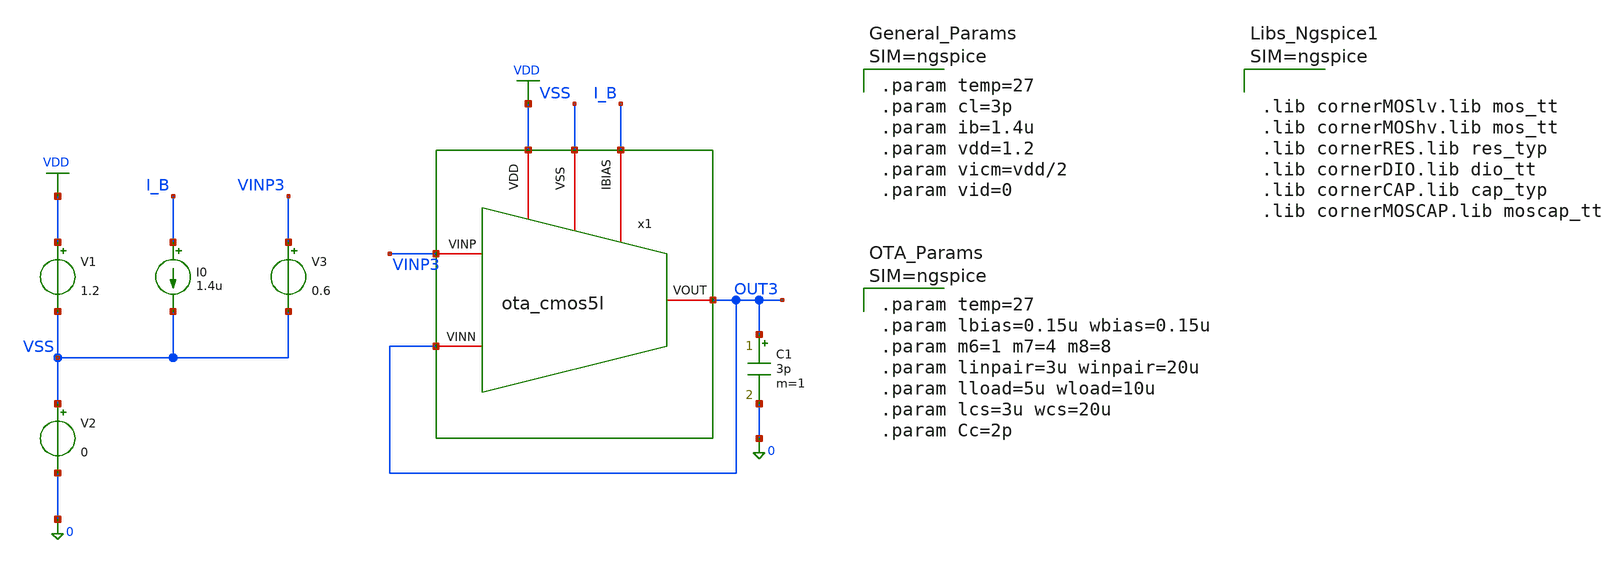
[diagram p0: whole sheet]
** sch_path: xschem/ota_cmos5l/tb/tb_ota_cmos5l_cmrr/tb_ota_cmos5l_cmrr.sch
**.subckt tb_ota_cmos5l_cmrr
x1 VSS I_B VDD OUT3 VINP3 OUT3 ota_cmos5l
C1 OUT3 0 3p m=1
I0 I_B VSS 1.4u
V1 VDD VSS 1.2
V2 VSS 0 0
V3 VINP3 VSS 0.6
**** begin user architecture code



.lib cornerMOSlv.lib mos_tt
.lib cornerMOShv.lib mos_tt
.lib cornerRES.lib res_typ
.lib cornerDIO.lib dio_tt
.lib cornerCAP.lib cap_typ
.lib cornerMOSCAP.lib moscap_tt





.param temp=27
.param cl=3p
.param ib=1.4u
.param vdd=1.2
.param vicm=vdd/2
.param vid=0





.param temp=27
.param lbias=0.15u wbias=0.15u
.param m6=1 m7=4 m8=8
.param linpair=3u winpair=20u
.param lload=5u wload=10u
.param lcs=3u wcs=20u
.param Cc=2p





.control
save all
shell mkdir -p result

* CMRR
alter @v1[acmag]=0
alter @v3[acmag]=1

ac dec 20 1 10G

let v_diff_res = v(VINP3) - v(OUT3)
let cmrr_curve = db(1 / (v_diff_res + 1e-15))

meas ac cmrr_dc find cmrr_curve at=10
meas ac cmrr_100k find cmrr_curve at=100k
meas ac cmrr_1meg find cmrr_curve at=1MEG

write ./result/tb_cg_ota_cmrr.raw v_diff_res cmrr_curve

echo "======================================================="
echo "  CMRR @ DC / 10 Hz        : " $&cmrr_dc   " dB (Target: > 60 dB)"
echo "  CMRR @ 100 kHz           : " $&cmrr_100k " dB"
echo "  CMRR @ 1 MHz             : " $&cmrr_1meg " dB"
echo "======================================================="

plot cmrr_curve xlog
.endc


**** end user architecture code
**.ends

* expanding   symbol:  /foss/designs/sg13cmos5l_spma_ip__instramp/xschem/ota_cmos5l/ota_cmos5l.sym #
*+ of pins=6
** sym_path: xschem/output_buffer/ota_cmos5l.sym
** sch_path: xschem/output_buffer/ota_cmos5l.sch
.subckt ota_cmos5l VSS IBIAS VDD VINN VINP VOUT
*.iopin IBIAS
*.iopin VDD
*.iopin VSS
*.iopin VOUT
*.iopin VINP
*.iopin VINN
XM6 IBIAS IBIAS VDD VDD sg13_lv_pmos w={wbias} l={lbias} ng=1 m={m6} mm_ok=1
XM7 net1 IBIAS VDD VDD sg13_lv_pmos w={wbias} l={lbias} ng=1 m={m7} mm_ok=1
XM8 VOUT IBIAS VDD VDD sg13_lv_pmos w={wbias} l={lbias} ng=1 m={m8} mm_ok=1
XM1 net2 VINN net1 VDD sg13_lv_pmos w={winpair} l={linpair} ng=1 m=1 mm_ok=1
XM2 net3 VINP net1 VDD sg13_lv_pmos w={winpair} l={linpair} ng=1 m=1 mm_ok=1
XM3 net2 net2 VSS VSS sg13_lv_nmos w={wload} l={lload} ng=1 m=1 mm_ok=1
XM4 net3 net2 VSS VSS sg13_lv_nmos w={wload} l={lload} ng=1 m=1 mm_ok=1
XM5 VOUT net3 VSS VSS sg13_lv_nmos w={wcs} l={lcs} ng=1 m=1 mm_ok=1
XR1 net3 net4 VSS rhigh w=0.5e-6 l=1.95e-6 m=1 b=0 mm_ok=1
.save v(vinp)
.save v(vinn)
.save v(vout)
XC2 VOUT net4 cap_cmomi w=15e-6 l=15e-6 mmin=1 mmax=4 feed=double subblock=0 m=5 mm_ok=1
**** begin user architecture code


.param temp=27
.param lbias=0.15u wbias=0.15u
.param m6=1 m7=4 m8=8
.param linpair=3u winpair=20u
.param lload=5u wload=10u
.param lcs=3u wcs=20u
.param Cc=2p



**** end user architecture code
XC1 VOUT net4 cap_cmomi w=15e-6 l=15e-6 mmin=1 mmax=4 feed=double subblock=0 m=4 mm_ok=1
.ends

.GLOBAL VDD
.end
